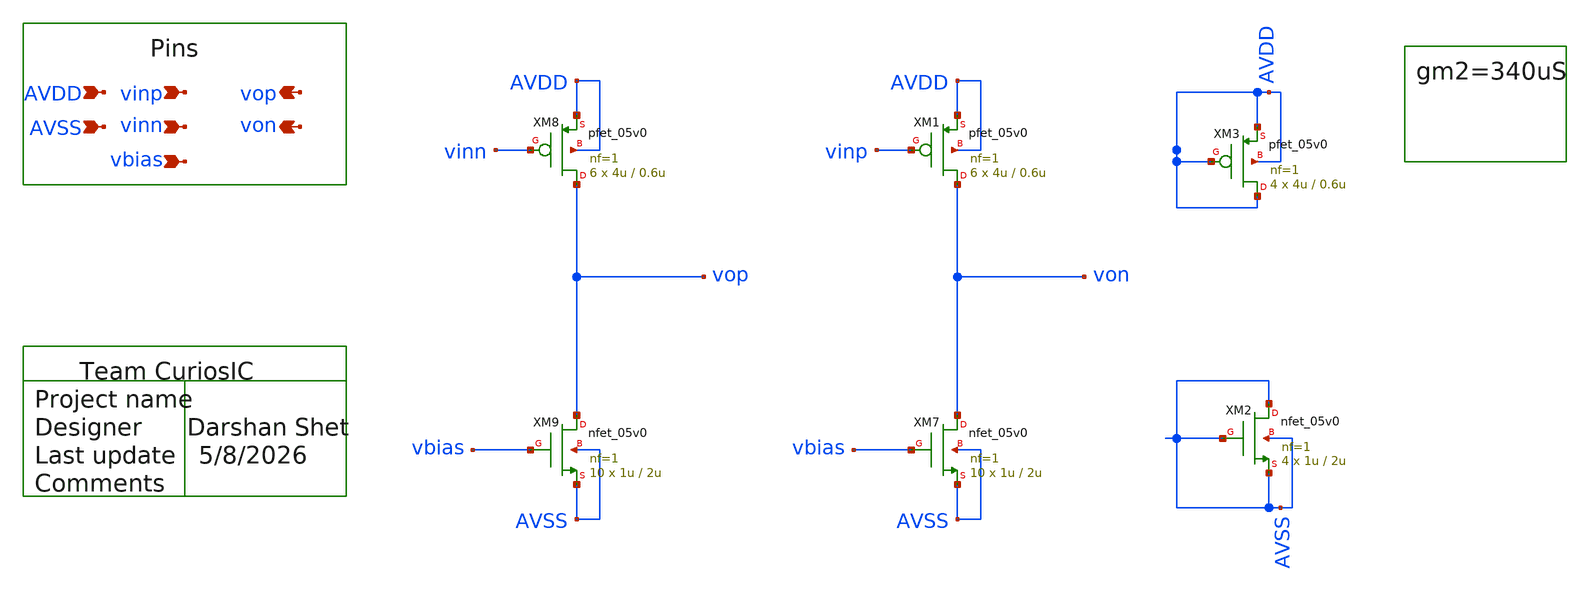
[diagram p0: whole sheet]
** sch_path: design/schematics/ADC/DSM_Loop_filter/First_int/OTA_Files/DS_cic_bms_afe_iadc_first_int_OTA_gm2.sch
**.subckt DS_cic_bms_afe_iadc_first_int_OTA_gm2 vinp vinn von vop AVDD AVSS vbias
*.ipin vinp
*.ipin vinn
*.opin von
*.opin vop
*.ipin AVDD
*.ipin AVSS
*.ipin vbias
XM1 von vinp AVDD AVDD pfet_05v0 L=0.6u W=4u nf=1 ad='int((nf+1)/2) * W/nf * 0.18u' as='int((nf+2)/2) * W/nf * 0.18u'
+ pd='2*int((nf+1)/2) * (W/nf + 0.18u)' ps='2*int((nf+2)/2) * (W/nf + 0.18u)' nrd='0.18u / W' nrs='0.18u / W'
+ sa=0 sb=0 sd=0 m=6
XM7 von vbias AVSS AVSS nfet_05v0 L=2u W=1u nf=1 ad='int((nf+1)/2) * W/nf * 0.18u' as='int((nf+2)/2) * W/nf * 0.18u'
+ pd='2*int((nf+1)/2) * (W/nf + 0.18u)' ps='2*int((nf+2)/2) * (W/nf + 0.18u)' nrd='0.18u / W' nrs='0.18u / W'
+ sa=0 sb=0 sd=0 m=10
XM8 vop vinn AVDD AVDD pfet_05v0 L=0.6u W=4u nf=1 ad='int((nf+1)/2) * W/nf * 0.18u' as='int((nf+2)/2) * W/nf * 0.18u'
+ pd='2*int((nf+1)/2) * (W/nf + 0.18u)' ps='2*int((nf+2)/2) * (W/nf + 0.18u)' nrd='0.18u / W' nrs='0.18u / W'
+ sa=0 sb=0 sd=0 m=6
XM9 vop vbias AVSS AVSS nfet_05v0 L=2u W=1u nf=1 ad='int((nf+1)/2) * W/nf * 0.18u' as='int((nf+2)/2) * W/nf * 0.18u'
+ pd='2*int((nf+1)/2) * (W/nf + 0.18u)' ps='2*int((nf+2)/2) * (W/nf + 0.18u)' nrd='0.18u / W' nrs='0.18u / W'
+ sa=0 sb=0 sd=0 m=10
XM2 AVSS AVSS AVSS AVSS nfet_05v0 L=2u W=1u nf=1 ad='int((nf+1)/2) * W/nf * 0.18u' as='int((nf+2)/2) * W/nf * 0.18u'
+ pd='2*int((nf+1)/2) * (W/nf + 0.18u)' ps='2*int((nf+2)/2) * (W/nf + 0.18u)' nrd='0.18u / W' nrs='0.18u / W'
+ sa=0 sb=0 sd=0 m=4
XM3 AVDD AVDD AVDD AVDD pfet_05v0 L=0.6u W=4u nf=1 ad='int((nf+1)/2) * W/nf * 0.18u' as='int((nf+2)/2) * W/nf * 0.18u'
+ pd='2*int((nf+1)/2) * (W/nf + 0.18u)' ps='2*int((nf+2)/2) * (W/nf + 0.18u)' nrd='0.18u / W' nrs='0.18u / W'
+ sa=0 sb=0 sd=0 m=4
**.ends
.end
